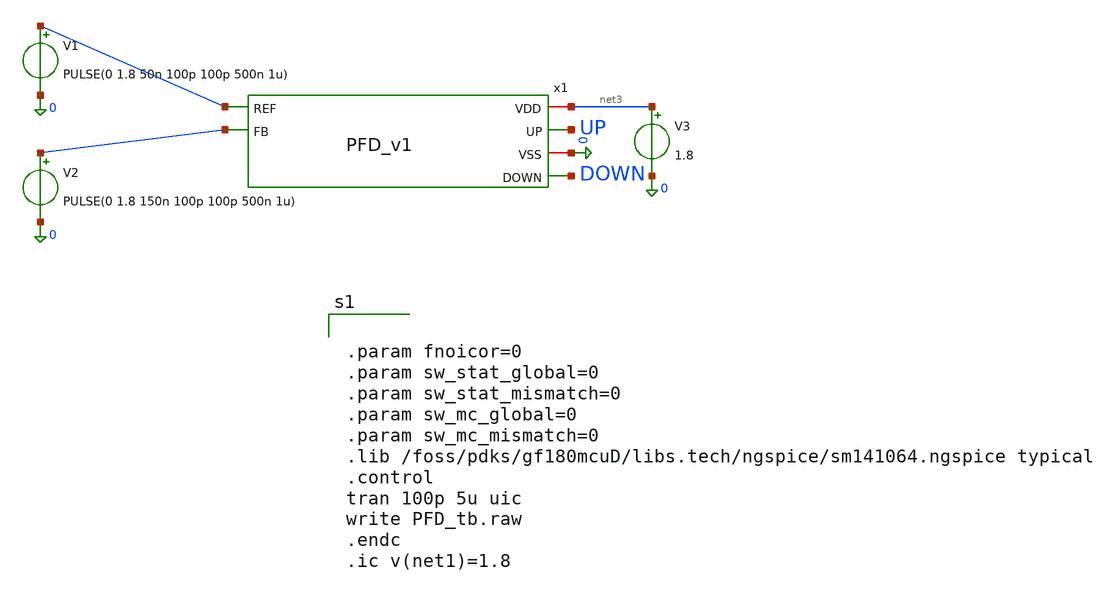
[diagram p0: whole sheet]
** sch_path: team_src/xschem/PFD_tb.sch
**.subckt PFD_tb
x1 net3 UP net1 0 DOWN net2 PFD_v1
V1 net1 0 PULSE(0 1.8 50n 100p 100p 500n 1u)
V2 net2 0 PULSE(0 1.8 150n 100p 100p 500n 1u)
V3 net3 0 1.8
**** begin user architecture code


.param fnoicor=0
.param sw_stat_global=0
.param sw_stat_mismatch=0
.param sw_mc_global=0
.param sw_mc_mismatch=0
.lib /foss/pdks/gf180mcuD/libs.tech/ngspice/sm141064.ngspice typical
.control
tran 100p 5u uic
write PFD_tb.raw
.endc
.ic v(net1)=1.8


**** end user architecture code
**.ends

* expanding   symbol:  PFD_v1.sym # of pins=6
** sym_path: team_src/xschem/PFD_v1.sym
** sch_path: team_src/xschem/PFD_v1.sch
.subckt PFD_v1 VDD UP REF VSS DOWN FB
*.ipin REF
*.iopin VSS
*.iopin VDD
*.opin UP
*.ipin FB
*.opin DOWN
x3 VDD net1 UP DOWN VSS NAND_v1
x1 net1 VDD VDD UP REF net2 VSS D_FF_RST_v1
x2 net1 VDD VDD DOWN FB net3 VSS D_FF_RST_v1
.ends


* expanding   symbol:  NAND_v1.sym # of pins=5
** sym_path: team_src/xschem/NAND_v1.sym
** sch_path: team_src/xschem/NAND_v1.sch
.subckt NAND_v1 VDD Y A B VSS
*.iopin VSS
*.iopin VDD
*.ipin A
*.opin Y
*.ipin B
XM1 net1 B VSS VSS nfet_03v3 L=0.28u W=1u nf=1 ad='int((nf+1)/2) * W/nf * 0.18u' as='int((nf+2)/2) * W/nf * 0.18u'
+ pd='2*int((nf+1)/2) * (W/nf + 0.18u)' ps='2*int((nf+2)/2) * (W/nf + 0.18u)' nrd='0.18u / W' nrs='0.18u / W'
+ sa=0 sb=0 sd=0 m=1
XM2 Y A net1 VSS nfet_03v3 L=0.28u W=1u nf=1 ad='int((nf+1)/2) * W/nf * 0.18u' as='int((nf+2)/2) * W/nf * 0.18u'
+ pd='2*int((nf+1)/2) * (W/nf + 0.18u)' ps='2*int((nf+2)/2) * (W/nf + 0.18u)' nrd='0.18u / W' nrs='0.18u / W'
+ sa=0 sb=0 sd=0 m=1
XM3 Y B VDD VDD pfet_03v3 L=0.28u W=1u nf=1 ad='int((nf+1)/2) * W/nf * 0.18u' as='int((nf+2)/2) * W/nf * 0.18u'
+ pd='2*int((nf+1)/2) * (W/nf + 0.18u)' ps='2*int((nf+2)/2) * (W/nf + 0.18u)' nrd='0.18u / W' nrs='0.18u / W'
+ sa=0 sb=0 sd=0 m=1
XM4 Y A VDD VDD pfet_03v3 L=0.28u W=1u nf=1 ad='int((nf+1)/2) * W/nf * 0.18u' as='int((nf+2)/2) * W/nf * 0.18u'
+ pd='2*int((nf+1)/2) * (W/nf + 0.18u)' ps='2*int((nf+2)/2) * (W/nf + 0.18u)' nrd='0.18u / W' nrs='0.18u / W'
+ sa=0 sb=0 sd=0 m=1
.ends


* expanding   symbol:  D_FF_RST_v1.sym # of pins=7
** sym_path: team_src/xschem/D_FF_RST_v1.sym
** sch_path: team_src/xschem/D_FF_RST_v1.sch
.subckt D_FF_RST_v1 RST VDD D Q CLK !Q VSS
*.ipin CLK
*.ipin D
*.iopin VDD
*.opin Q
*.opin !Q
*.iopin VSS
*.ipin RST
x1 VDD Q net5 !Q VSS NAND_v1
x3 VDD net7 D net2 VSS NAND_v1
x4 VDD net6 net1 net2 VSS NAND_v1
x5 VDD D net1 VSS NOT_v1
x6 VDD net3 net2 VSS NOT_v1
x7 VDD CLK net4 VSS NOT_v1
x8 VDD net3 CLK net4 VSS NAND_v1
x2 RST VDD !Q Q net6 VSS NAND3_v1
x9 VDD net7 net8 VSS NOT_v1
x10 VDD net5 net8 RST VSS NAND_v1
.ends


* expanding   symbol:  NOT_v1.sym # of pins=4
** sym_path: team_src/xschem/NOT_v1.sym
** sch_path: team_src/xschem/NOT_v1.sch
.subckt NOT_v1 VDD A Y VSS
*.iopin VSS
*.iopin VDD
*.ipin A
*.opin Y
XM2 Y A VSS VSS nfet_03v3 L=0.28u W=1u nf=1 ad='int((nf+1)/2) * W/nf * 0.18u' as='int((nf+2)/2) * W/nf * 0.18u'
+ pd='2*int((nf+1)/2) * (W/nf + 0.18u)' ps='2*int((nf+2)/2) * (W/nf + 0.18u)' nrd='0.18u / W' nrs='0.18u / W'
+ sa=0 sb=0 sd=0 m=1
XM4 Y A VDD VDD pfet_03v3 L=0.28u W=1u nf=1 ad='int((nf+1)/2) * W/nf * 0.18u' as='int((nf+2)/2) * W/nf * 0.18u'
+ pd='2*int((nf+1)/2) * (W/nf + 0.18u)' ps='2*int((nf+2)/2) * (W/nf + 0.18u)' nrd='0.18u / W' nrs='0.18u / W'
+ sa=0 sb=0 sd=0 m=1
.ends


* expanding   symbol:  NAND3_v1.sym # of pins=6
** sym_path: team_src/xschem/NAND3_v1.sym
** sch_path: team_src/xschem/NAND3_v1.sch
.subckt NAND3_v1 C VDD Y A B VSS
*.iopin VSS
*.iopin VDD
*.ipin A
*.opin Y
*.ipin B
*.ipin C
XM1 net1 B net2 VSS nfet_03v3 L=0.28u W=3u nf=1 ad='int((nf+1)/2) * W/nf * 0.18u' as='int((nf+2)/2) * W/nf * 0.18u'
+ pd='2*int((nf+1)/2) * (W/nf + 0.18u)' ps='2*int((nf+2)/2) * (W/nf + 0.18u)' nrd='0.18u / W' nrs='0.18u / W'
+ sa=0 sb=0 sd=0 m=1
XM2 Y A net1 VSS nfet_03v3 L=0.28u W=3u nf=1 ad='int((nf+1)/2) * W/nf * 0.18u' as='int((nf+2)/2) * W/nf * 0.18u'
+ pd='2*int((nf+1)/2) * (W/nf + 0.18u)' ps='2*int((nf+2)/2) * (W/nf + 0.18u)' nrd='0.18u / W' nrs='0.18u / W'
+ sa=0 sb=0 sd=0 m=1
XM3 Y B VDD VDD pfet_03v3 L=0.28u W=1u nf=1 ad='int((nf+1)/2) * W/nf * 0.18u' as='int((nf+2)/2) * W/nf * 0.18u'
+ pd='2*int((nf+1)/2) * (W/nf + 0.18u)' ps='2*int((nf+2)/2) * (W/nf + 0.18u)' nrd='0.18u / W' nrs='0.18u / W'
+ sa=0 sb=0 sd=0 m=1
XM4 Y A VDD VDD pfet_03v3 L=0.28u W=1u nf=1 ad='int((nf+1)/2) * W/nf * 0.18u' as='int((nf+2)/2) * W/nf * 0.18u'
+ pd='2*int((nf+1)/2) * (W/nf + 0.18u)' ps='2*int((nf+2)/2) * (W/nf + 0.18u)' nrd='0.18u / W' nrs='0.18u / W'
+ sa=0 sb=0 sd=0 m=1
XM5 Y C VDD VDD pfet_03v3 L=0.28u W=1u nf=1 ad='int((nf+1)/2) * W/nf * 0.18u' as='int((nf+2)/2) * W/nf * 0.18u'
+ pd='2*int((nf+1)/2) * (W/nf + 0.18u)' ps='2*int((nf+2)/2) * (W/nf + 0.18u)' nrd='0.18u / W' nrs='0.18u / W'
+ sa=0 sb=0 sd=0 m=1
XM6 net2 C VSS VSS nfet_03v3 L=0.28u W=3u nf=1 ad='int((nf+1)/2) * W/nf * 0.18u' as='int((nf+2)/2) * W/nf * 0.18u'
+ pd='2*int((nf+1)/2) * (W/nf + 0.18u)' ps='2*int((nf+2)/2) * (W/nf + 0.18u)' nrd='0.18u / W' nrs='0.18u / W'
+ sa=0 sb=0 sd=0 m=1
.ends

.end
